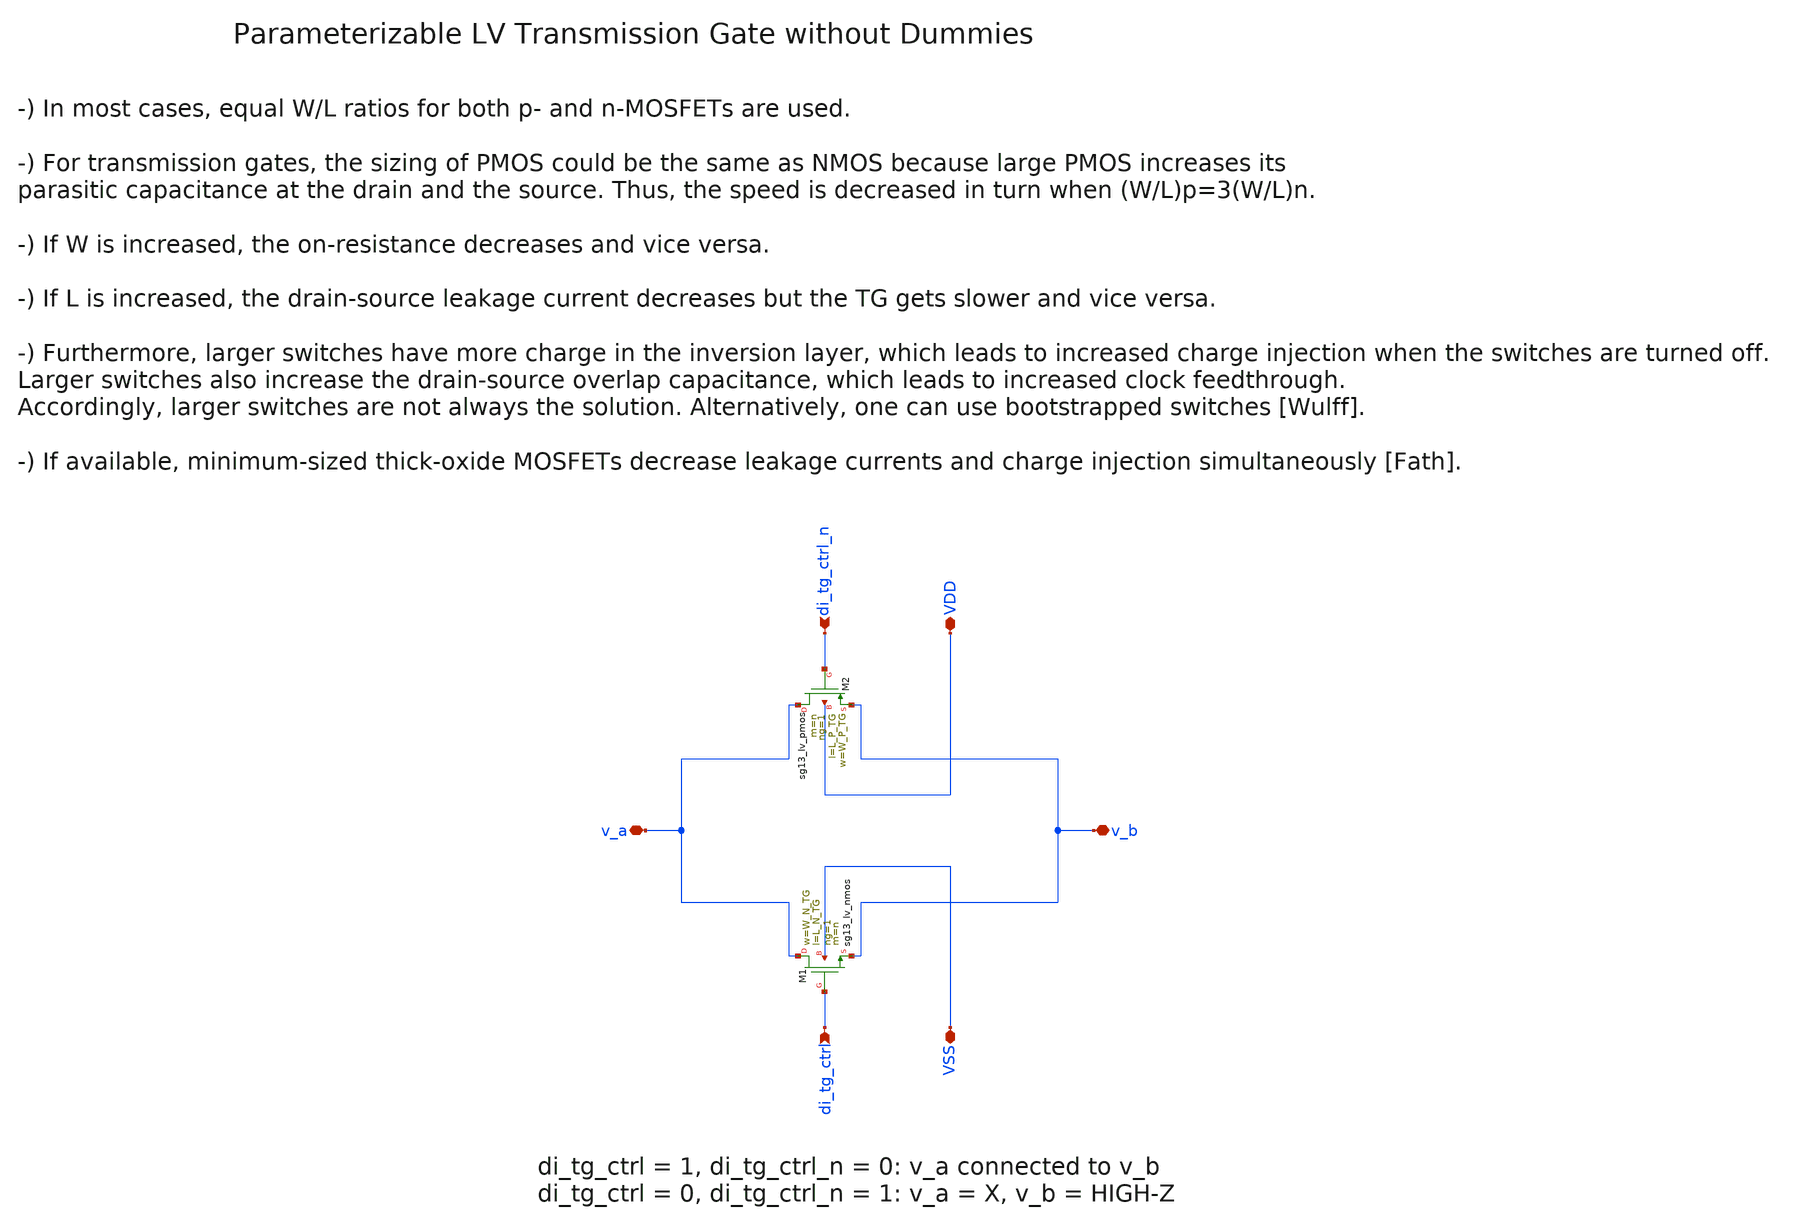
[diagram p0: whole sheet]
** sch_path: xschem/transmission_gate/transmission_gate_lv_wo_dummy.sch
**.subckt transmission_gate_lv_wo_dummy v_a v_b VDD VSS di_tg_ctrl di_tg_ctrl_n
*.iopin v_a
*.iopin v_b
*.iopin VDD
*.iopin VSS
*.ipin di_tg_ctrl
*.ipin di_tg_ctrl_n
XM1 v_a di_tg_ctrl v_b VSS sg13_lv_nmos w=W_N_TG l=L_N_TG ng=1 m=n mm_ok=1
XM2 v_a di_tg_ctrl_n v_b VDD sg13_lv_pmos w=W_P_TG l=L_P_TG ng=1 m=n mm_ok=1
**.ends
.end
